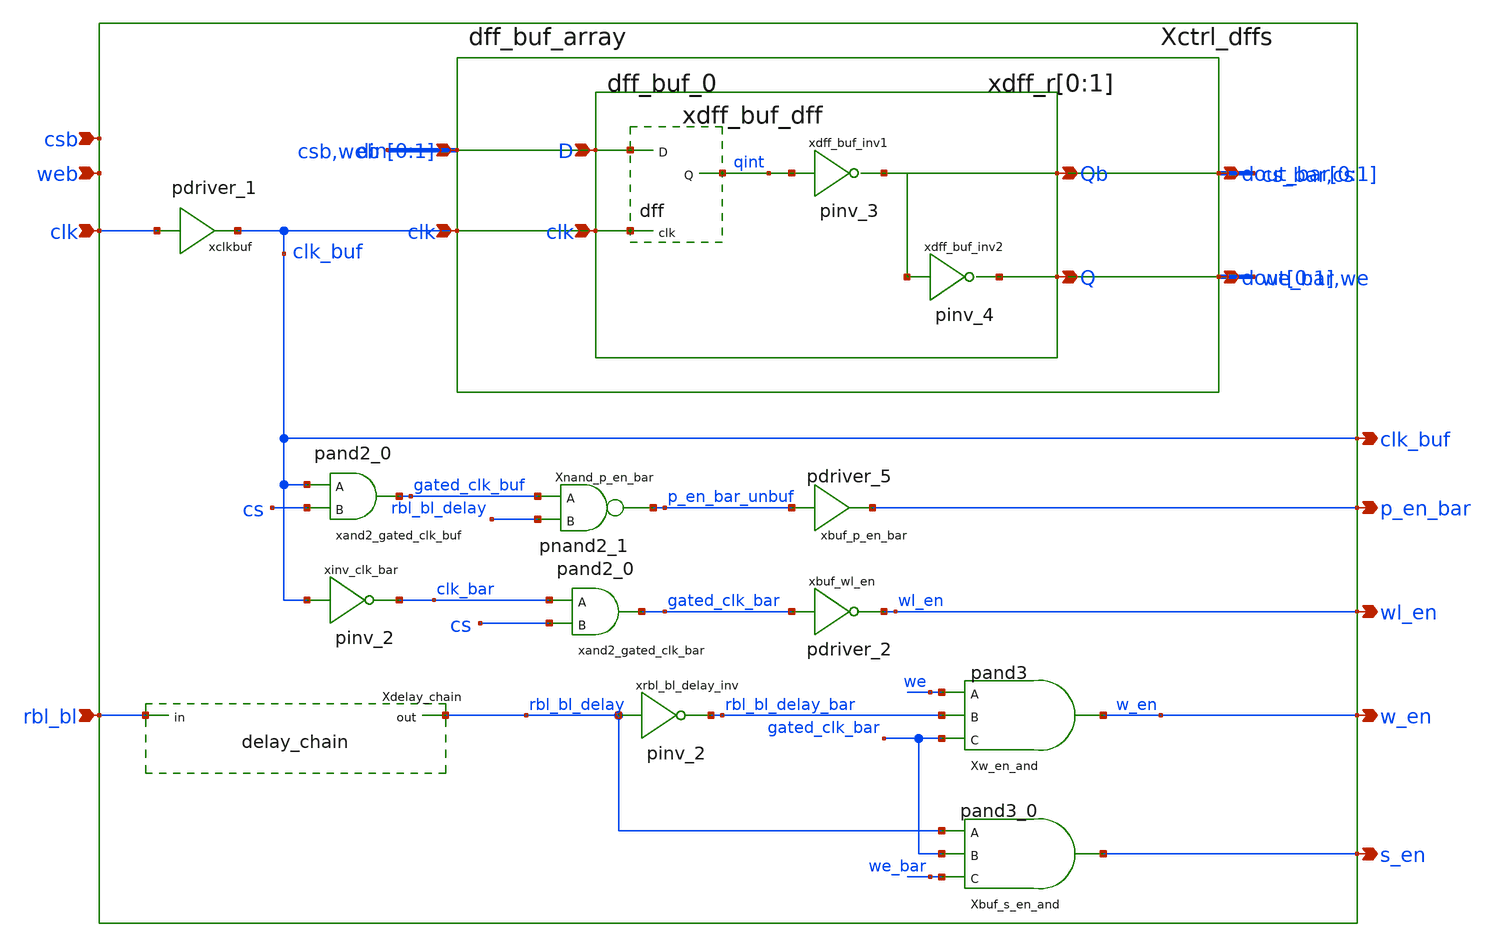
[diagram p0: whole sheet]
** sch_path: sram_2_64_scn4m/control_logic_rw.sch
**.subckt control_logic_rw clk rbl_bl s_en w_en p_en_bar wl_en csb web clk_buf
*.ipin clk
*.ipin rbl_bl
*.opin s_en
*.opin w_en
*.opin p_en_bar
*.opin wl_en
*.ipin csb
*.ipin web
*.opin clk_buf
xclkbuf clk clk_buf vdd gnd pdriver_1
xinv_clk_bar clk_buf clk_bar vdd gnd pinv_2
xand2_gated_clk_bar clk_bar cs gated_clk_bar vdd gnd pand2_0
xand2_gated_clk_buf clk_buf cs gated_clk_buf vdd gnd pand2_0
xbuf_wl_en gated_clk_bar wl_en vdd gnd pdriver_2
xrbl_bl_delay_inv rbl_bl_delay rbl_bl_delay_bar vdd gnd pinv_2
Xw_en_and we rbl_bl_delay_bar gated_clk_bar w_en vdd gnd pand3
Xbuf_s_en_and rbl_bl_delay gated_clk_bar we_bar s_en vdd gnd pand3_0
Xdelay_chain rbl_bl rbl_bl_delay vdd gnd delay_chain
Xnand_p_en_bar gated_clk_buf rbl_bl_delay p_en_bar_unbuf vdd gnd pnand2_1
xbuf_p_en_bar p_en_bar_unbuf p_en_bar pdriver_5
Xctrl_dffs csb web we_bar we cs_bar cs clk_buf vdd gnd dff_buf_array
**.ends
.end
